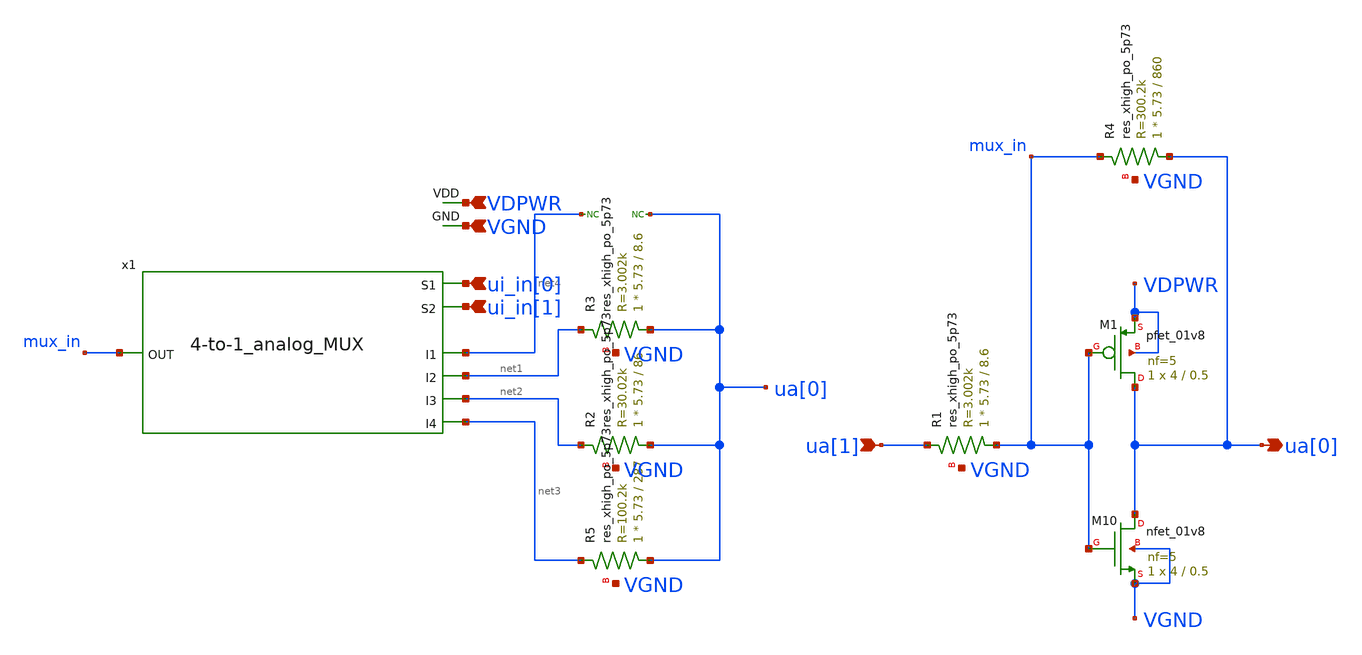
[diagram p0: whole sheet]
** sch_path: xschem/mixedsignal_final.sch
**.subckt mixedsignal_final ua[0] ua[1] ui_in[0] ui_in[1] VDPWR VGND
*.opin ua[0]
*.ipin ua[1]
*.ipin ui_in[0]
*.ipin ui_in[1]
*.ipin VDPWR
*.ipin VGND
x1 ui_in[0] ui_in[1] VDPWR VGND net4 net1 mux_in net2 net3 4-to-1_analog_MUX
* noconn ua[0]
* noconn #net4
XR3 ua[0] net1 VGND sky130_fd_pr__res_xhigh_po_5p73 L=8.6 mult=1 m=1
XR2 ua[0] net2 VGND sky130_fd_pr__res_xhigh_po_5p73 L=86 mult=1 m=1
XR4 ua[0] mux_in VGND sky130_fd_pr__res_xhigh_po_5p73 L=860 mult=1 m=1
XR1 mux_in ua[1] VGND sky130_fd_pr__res_xhigh_po_5p73 L=8.6 mult=1 m=1
XR5 ua[0] net3 VGND sky130_fd_pr__res_xhigh_po_5p73 L=287 mult=1 m=1
XM1 ua[0] mux_in VDPWR VDPWR sky130_fd_pr__pfet_01v8 L=0.5 W=4 nf=5 ad='int((nf+1)/2) * W/nf * 0.29'
+ as='int((nf+2)/2) * W/nf * 0.29' pd='2*int((nf+1)/2) * (W/nf + 0.29)' ps='2*int((nf+2)/2) * (W/nf + 0.29)'
+ nrd='0.29 / W' nrs='0.29 / W' sa=0 sb=0 sd=0 mult=1 m=1
XM10 ua[0] mux_in VGND VGND sky130_fd_pr__nfet_01v8 L=0.5 W=4 nf=5 ad='int((nf+1)/2) * W/nf * 0.29' as='int((nf+2)/2) * W/nf * 0.29'
+ pd='2*int((nf+1)/2) * (W/nf + 0.29)' ps='2*int((nf+2)/2) * (W/nf + 0.29)' nrd='0.29 / W' nrs='0.29 / W'
+ sa=0 sb=0 sd=0 mult=1 m=1
**.ends

* expanding   symbol:  4-to-1_analog_MUX.sym # of pins=9
** sym_path: xschem/4-to-1_analog_MUX.sym
** sch_path: xschem/4-to-1_analog_MUX.sch
.subckt 4-to-1_analog_MUX S1 S2 VDD GND I1 I2 OUT I3 I4
*.ipin I1
*.ipin I2
*.ipin I3
*.ipin I4
*.opin OUT
*.ipin S1
*.ipin S2
*.ipin VDD
*.ipin GND
x1 S1 S1bar GND VDD Inverter
x2 S2 S2bar GND VDD Inverter
XM9 net1 S2 OUT VDD sky130_fd_pr__pfet_01v8 L=0.5 W=1 nf=1 ad='int((nf+1)/2) * W/nf * 0.29' as='int((nf+2)/2) * W/nf * 0.29'
+ pd='2*int((nf+1)/2) * (W/nf + 0.29)' ps='2*int((nf+2)/2) * (W/nf + 0.29)' nrd='0.29 / W' nrs='0.29 / W'
+ sa=0 sb=0 sd=0 mult=1 m=1
XM1 I1 S1 net1 VDD sky130_fd_pr__pfet_01v8 L=0.5 W=1 nf=1 ad='int((nf+1)/2) * W/nf * 0.29' as='int((nf+2)/2) * W/nf * 0.29'
+ pd='2*int((nf+1)/2) * (W/nf + 0.29)' ps='2*int((nf+2)/2) * (W/nf + 0.29)' nrd='0.29 / W' nrs='0.29 / W'
+ sa=0 sb=0 sd=0 mult=1 m=1
XM2 I3 S1bar net1 VDD sky130_fd_pr__pfet_01v8 L=0.5 W=1 nf=1 ad='int((nf+1)/2) * W/nf * 0.29' as='int((nf+2)/2) * W/nf * 0.29'
+ pd='2*int((nf+1)/2) * (W/nf + 0.29)' ps='2*int((nf+2)/2) * (W/nf + 0.29)' nrd='0.29 / W' nrs='0.29 / W'
+ sa=0 sb=0 sd=0 mult=1 m=1
XM5 I2 S1 net2 VDD sky130_fd_pr__pfet_01v8 L=0.5 W=1 nf=1 ad='int((nf+1)/2) * W/nf * 0.29' as='int((nf+2)/2) * W/nf * 0.29'
+ pd='2*int((nf+1)/2) * (W/nf + 0.29)' ps='2*int((nf+2)/2) * (W/nf + 0.29)' nrd='0.29 / W' nrs='0.29 / W'
+ sa=0 sb=0 sd=0 mult=1 m=1
XM7 I4 S1bar net2 VDD sky130_fd_pr__pfet_01v8 L=0.5 W=1 nf=1 ad='int((nf+1)/2) * W/nf * 0.29' as='int((nf+2)/2) * W/nf * 0.29'
+ pd='2*int((nf+1)/2) * (W/nf + 0.29)' ps='2*int((nf+2)/2) * (W/nf + 0.29)' nrd='0.29 / W' nrs='0.29 / W'
+ sa=0 sb=0 sd=0 mult=1 m=1
XM11 net2 S2bar OUT VDD sky130_fd_pr__pfet_01v8 L=0.5 W=1 nf=1 ad='int((nf+1)/2) * W/nf * 0.29' as='int((nf+2)/2) * W/nf * 0.29'
+ pd='2*int((nf+1)/2) * (W/nf + 0.29)' ps='2*int((nf+2)/2) * (W/nf + 0.29)' nrd='0.29 / W' nrs='0.29 / W'
+ sa=0 sb=0 sd=0 mult=1 m=1
XM3 I1 S1bar net1 GND sky130_fd_pr__nfet_01v8 L=1 W=1 nf=1 ad='int((nf+1)/2) * W/nf * 0.29' as='int((nf+2)/2) * W/nf * 0.29'
+ pd='2*int((nf+1)/2) * (W/nf + 0.29)' ps='2*int((nf+2)/2) * (W/nf + 0.29)' nrd='0.29 / W' nrs='0.29 / W'
+ sa=0 sb=0 sd=0 mult=1 m=1
XM4 I3 S1 net1 GND sky130_fd_pr__nfet_01v8 L=1 W=1 nf=1 ad='int((nf+1)/2) * W/nf * 0.29' as='int((nf+2)/2) * W/nf * 0.29'
+ pd='2*int((nf+1)/2) * (W/nf + 0.29)' ps='2*int((nf+2)/2) * (W/nf + 0.29)' nrd='0.29 / W' nrs='0.29 / W'
+ sa=0 sb=0 sd=0 mult=1 m=1
XM10 net1 S2bar OUT GND sky130_fd_pr__nfet_01v8 L=1 W=1 nf=1 ad='int((nf+1)/2) * W/nf * 0.29' as='int((nf+2)/2) * W/nf * 0.29'
+ pd='2*int((nf+1)/2) * (W/nf + 0.29)' ps='2*int((nf+2)/2) * (W/nf + 0.29)' nrd='0.29 / W' nrs='0.29 / W'
+ sa=0 sb=0 sd=0 mult=1 m=1
XM6 I2 S1bar net2 GND sky130_fd_pr__nfet_01v8 L=1 W=1 nf=1 ad='int((nf+1)/2) * W/nf * 0.29' as='int((nf+2)/2) * W/nf * 0.29'
+ pd='2*int((nf+1)/2) * (W/nf + 0.29)' ps='2*int((nf+2)/2) * (W/nf + 0.29)' nrd='0.29 / W' nrs='0.29 / W'
+ sa=0 sb=0 sd=0 mult=1 m=1
XM8 I4 S1 net2 GND sky130_fd_pr__nfet_01v8 L=1 W=1 nf=1 ad='int((nf+1)/2) * W/nf * 0.29' as='int((nf+2)/2) * W/nf * 0.29'
+ pd='2*int((nf+1)/2) * (W/nf + 0.29)' ps='2*int((nf+2)/2) * (W/nf + 0.29)' nrd='0.29 / W' nrs='0.29 / W'
+ sa=0 sb=0 sd=0 mult=1 m=1
XM12 net2 S2 OUT GND sky130_fd_pr__nfet_01v8 L=1 W=1 nf=1 ad='int((nf+1)/2) * W/nf * 0.29' as='int((nf+2)/2) * W/nf * 0.29'
+ pd='2*int((nf+1)/2) * (W/nf + 0.29)' ps='2*int((nf+2)/2) * (W/nf + 0.29)' nrd='0.29 / W' nrs='0.29 / W'
+ sa=0 sb=0 sd=0 mult=1 m=1
.ends


* expanding   symbol:  Inverter.sym # of pins=4
** sym_path: xschem/Inverter.sym
** sch_path: xschem/Inverter.sch
.subckt Inverter Vin Vout GND VDD
*.opin Vout
*.ipin Vin
*.ipin VDD
*.ipin GND
XM1 Vout Vin VDD VDD sky130_fd_pr__pfet_01v8 L=0.5 W=1 nf=1 ad='int((nf+1)/2) * W/nf * 0.29' as='int((nf+2)/2) * W/nf * 0.29'
+ pd='2*int((nf+1)/2) * (W/nf + 0.29)' ps='2*int((nf+2)/2) * (W/nf + 0.29)' nrd='0.29 / W' nrs='0.29 / W'
+ sa=0 sb=0 sd=0 mult=1 m=1
XM2 Vout Vin GND GND sky130_fd_pr__nfet_01v8 L=1 W=1 nf=1 ad='int((nf+1)/2) * W/nf * 0.29' as='int((nf+2)/2) * W/nf * 0.29'
+ pd='2*int((nf+1)/2) * (W/nf + 0.29)' ps='2*int((nf+2)/2) * (W/nf + 0.29)' nrd='0.29 / W' nrs='0.29 / W'
+ sa=0 sb=0 sd=0 mult=1 m=1
.ends

.end
